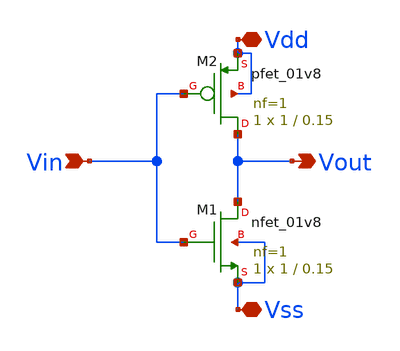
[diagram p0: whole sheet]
** sch_path: week1/designs/xschem/inv1.sch
**.subckt inv1 Vin Vout Vdd Vss
*.ipin Vin
*.opin Vout
*.iopin Vdd
*.iopin Vss
XM1 Vout Vin Vss Vss sky130_fd_pr__nfet_01v8 L=0.15 W=1 nf=1 ad='int((nf+1)/2) * W/nf * 0.29' as='int((nf+2)/2) * W/nf * 0.29'
+ pd='2*int((nf+1)/2) * (W/nf + 0.29)' ps='2*int((nf+2)/2) * (W/nf + 0.29)' nrd='0.29 / W' nrs='0.29 / W'
+ sa=0 sb=0 sd=0 mult=1 m=1
XM2 Vout Vin Vdd Vdd sky130_fd_pr__pfet_01v8 L=0.15 W=1 nf=1 ad='int((nf+1)/2) * W/nf * 0.29' as='int((nf+2)/2) * W/nf * 0.29'
+ pd='2*int((nf+1)/2) * (W/nf + 0.29)' ps='2*int((nf+2)/2) * (W/nf + 0.29)' nrd='0.29 / W' nrs='0.29 / W'
+ sa=0 sb=0 sd=0 mult=1 m=1
**.ends
.end
